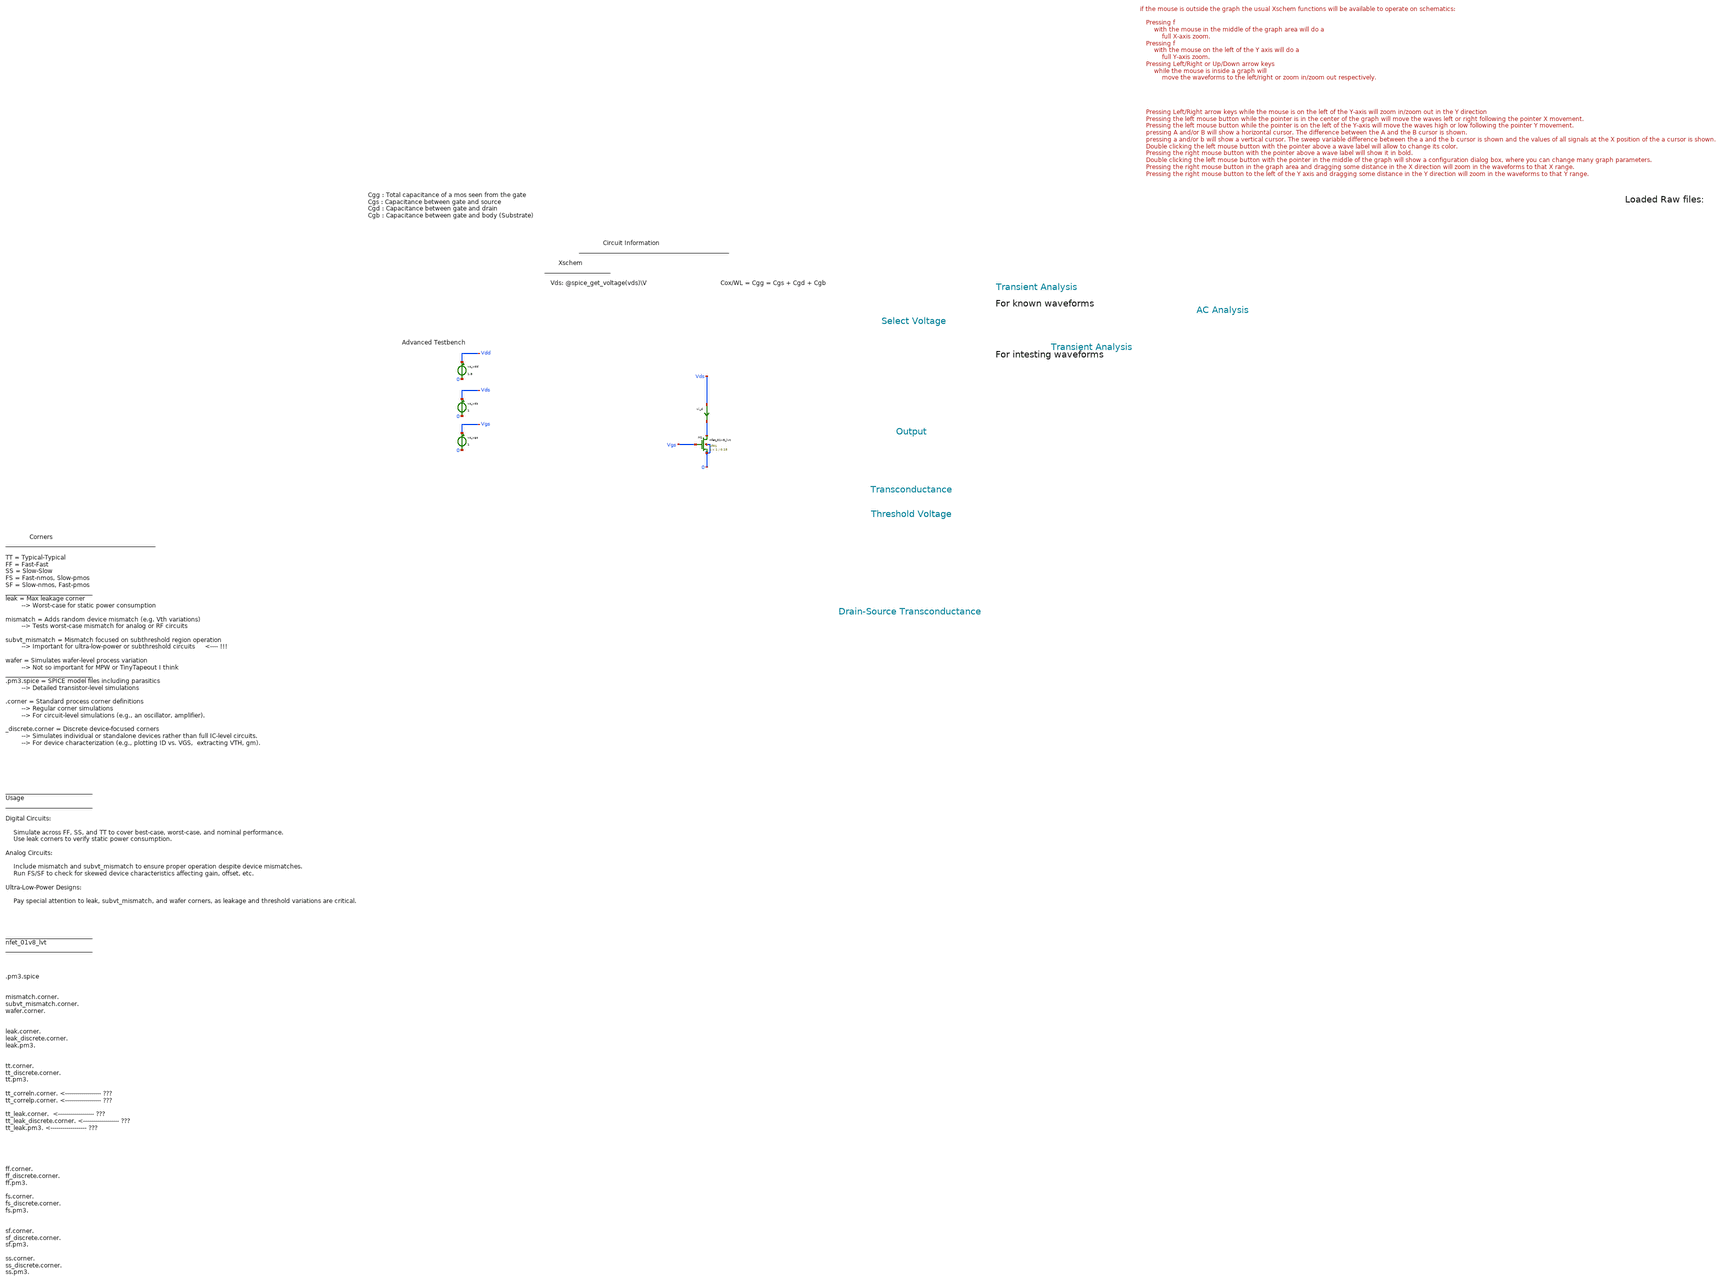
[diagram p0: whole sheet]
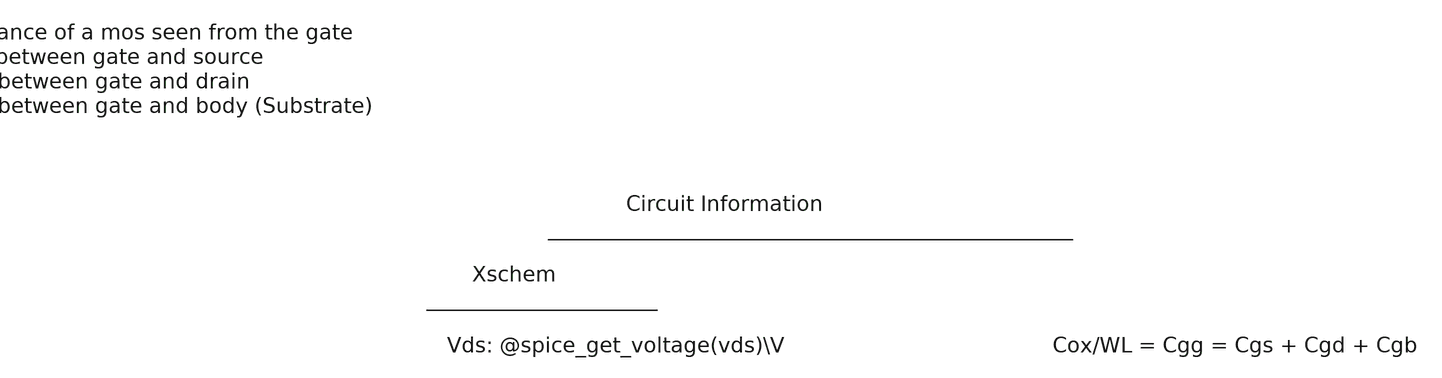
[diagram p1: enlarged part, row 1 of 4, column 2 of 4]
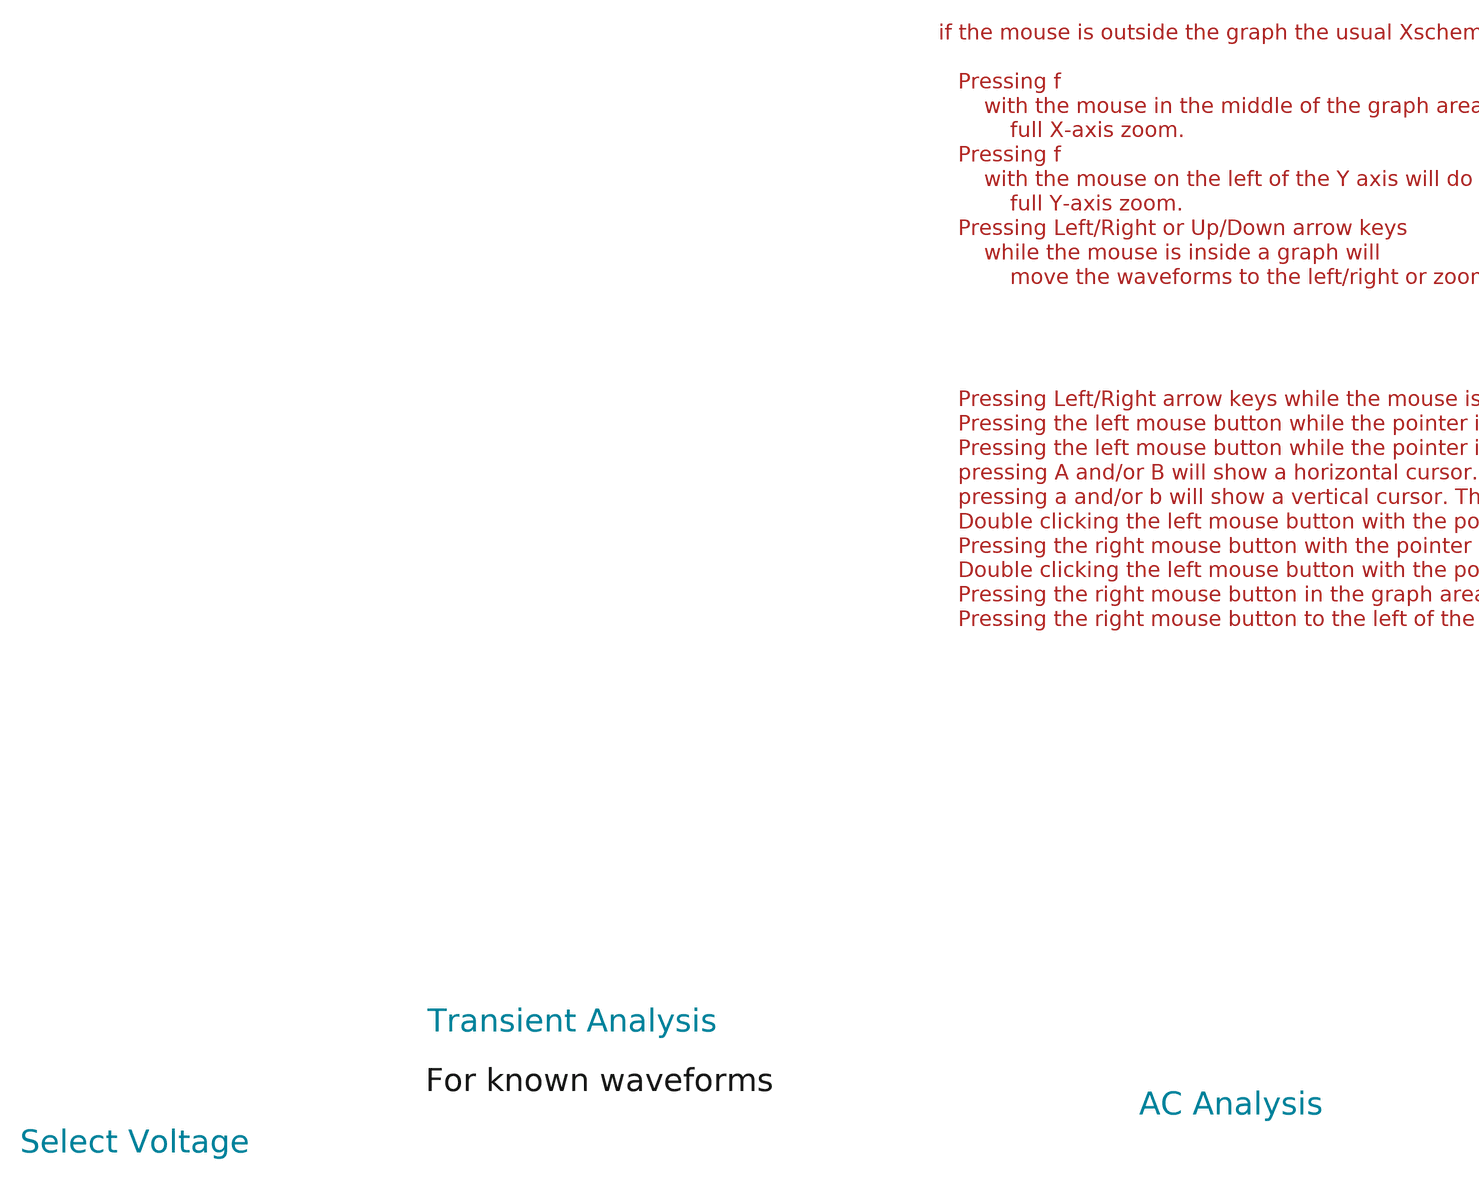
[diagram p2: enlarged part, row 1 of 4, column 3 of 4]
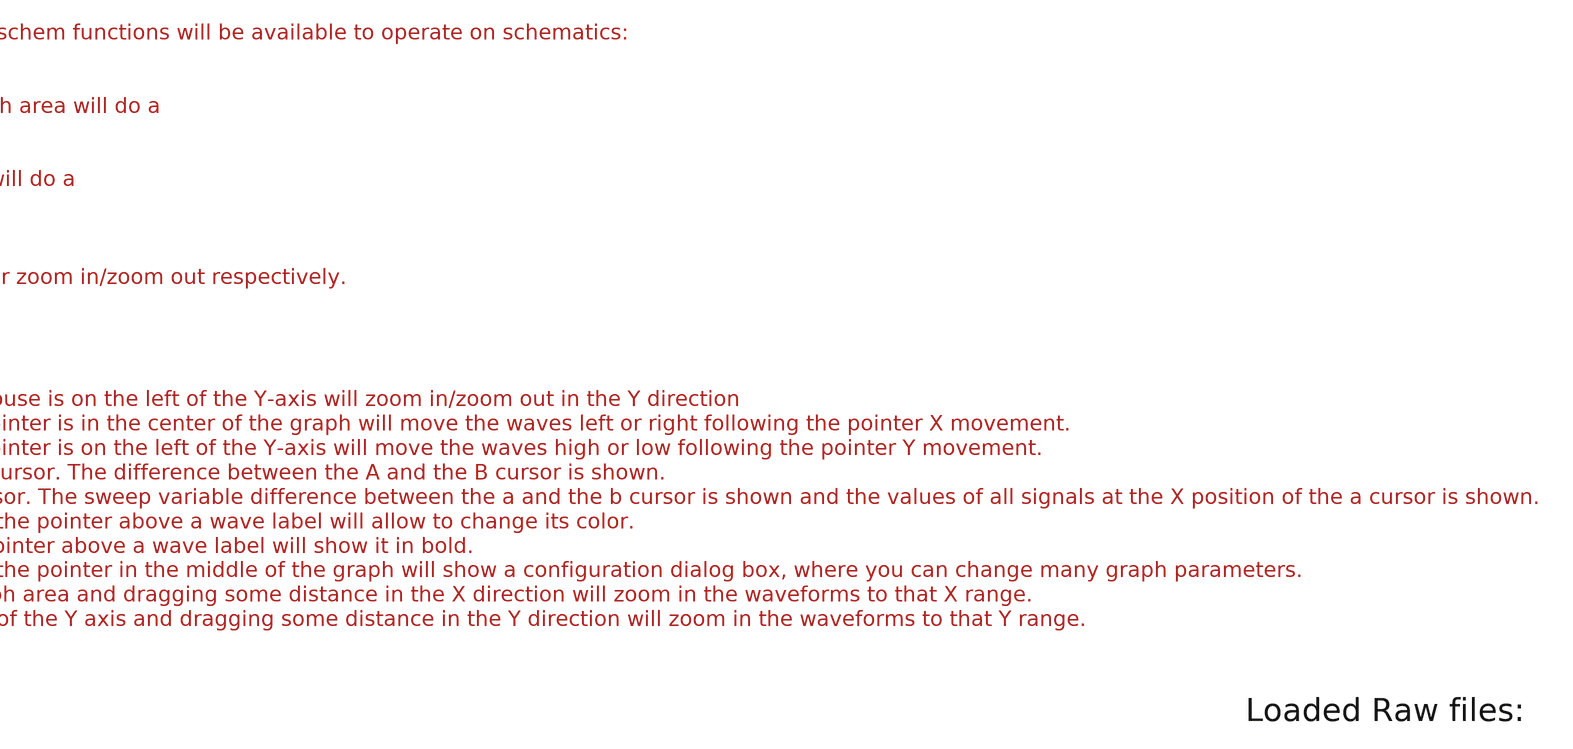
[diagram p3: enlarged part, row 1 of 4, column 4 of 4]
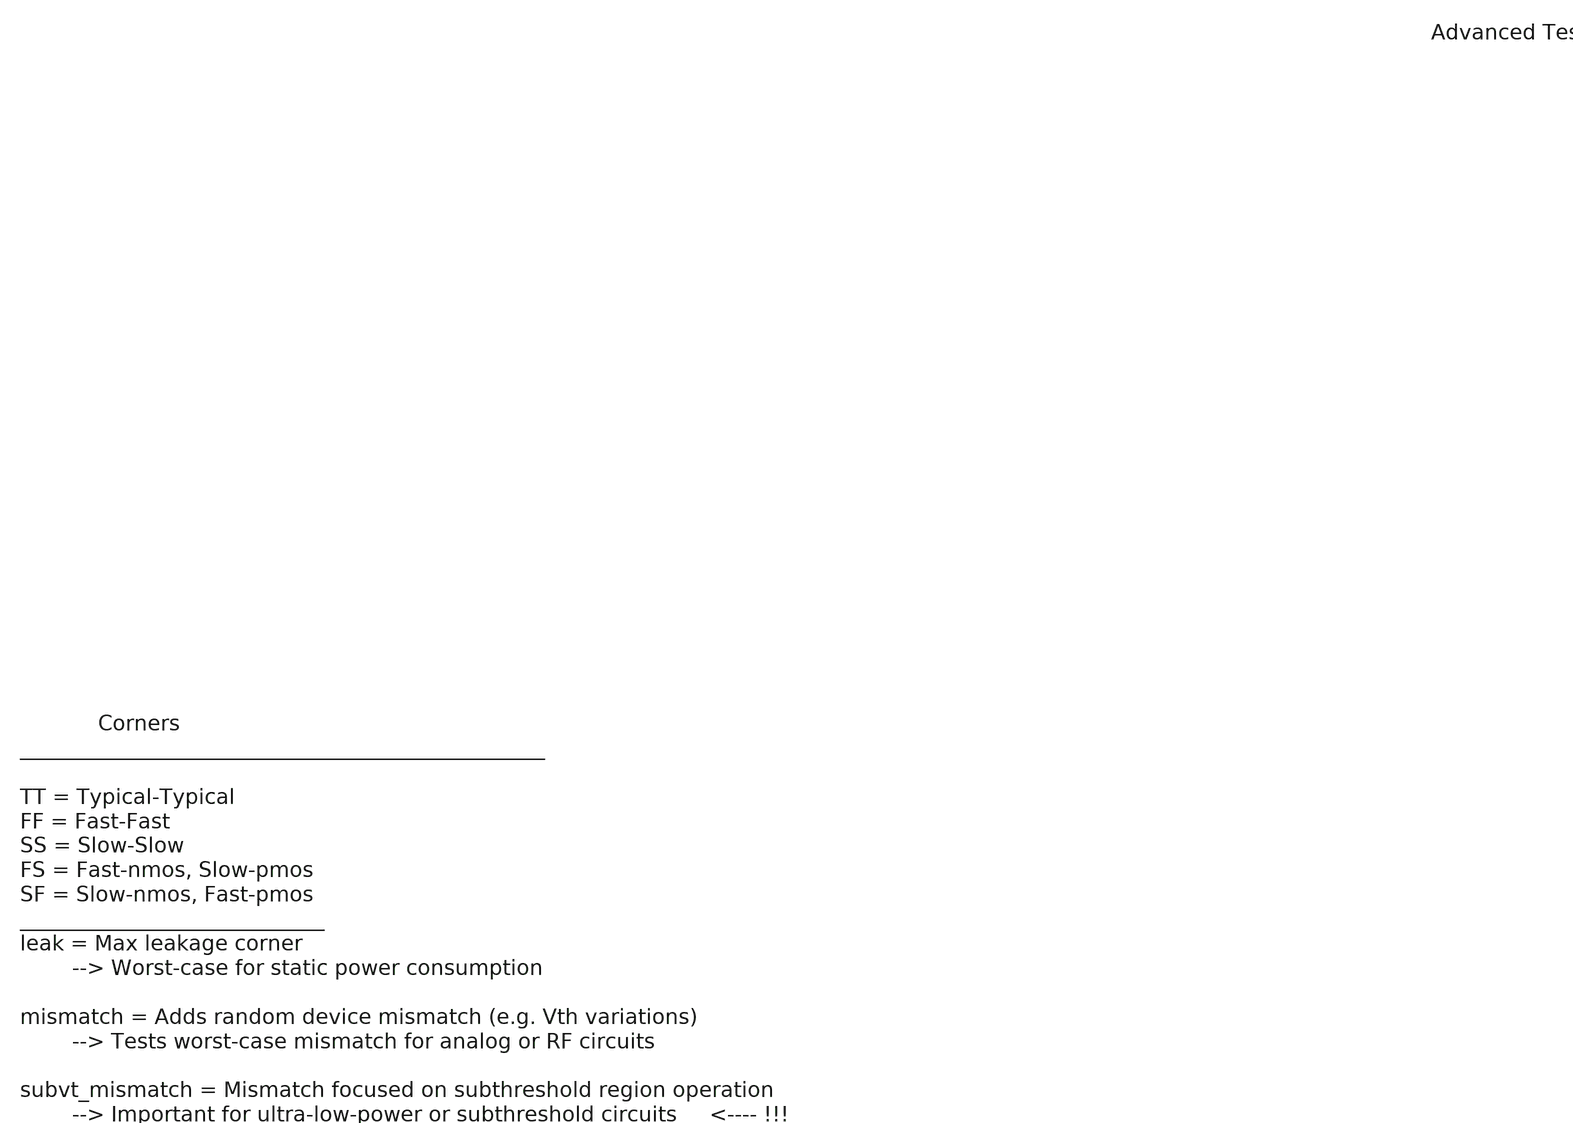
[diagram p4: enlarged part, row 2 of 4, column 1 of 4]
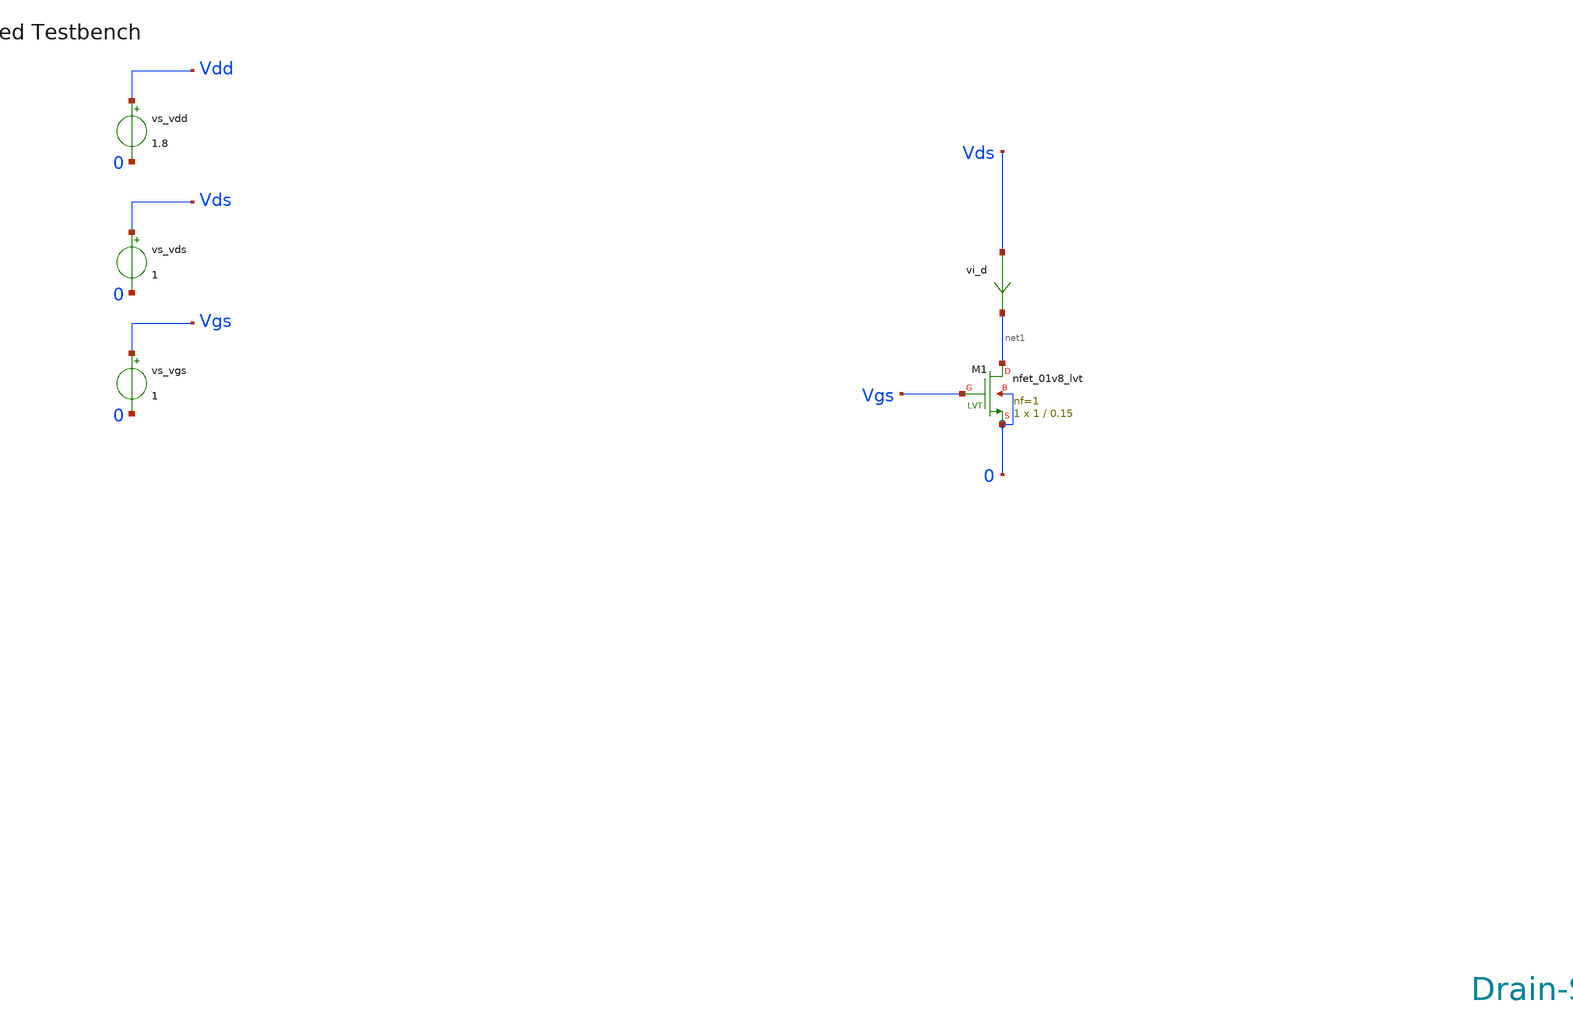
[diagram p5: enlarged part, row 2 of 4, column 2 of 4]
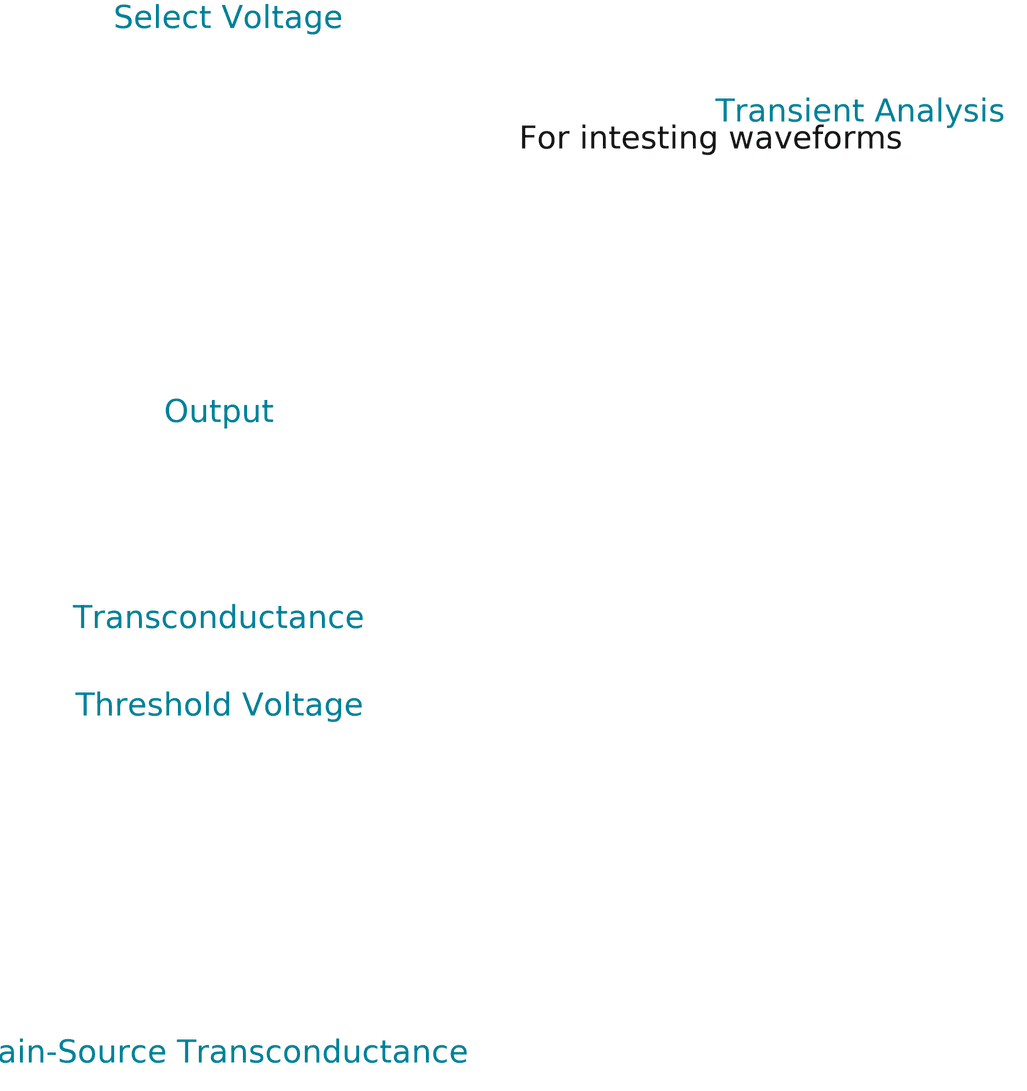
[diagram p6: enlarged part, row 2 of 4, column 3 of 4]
** sch_path: tt10-hdl/tt_um_test_commit/xschem/T0/nmos_lvt.sch
* Copyright (C) 1998-2024 Stefan Frederik Schippers
* This program is free software; you can redistribute it and/or modify
* it under the terms of the GNU General Public License as published by
* the Free Software Foundation; either version 2 of the License, or
* (at your option) any later version.
* This program is distributed in the hope that it will be useful,
* but WITHOUT ANY WARRANTY; without even the implied warranty of
* MERCHANTABILITY or FITNESS FOR A PARTICULAR PURPOSE.  See the
* GNU General Public License for more details.
* You should have received a copy of the GNU General Public License
* along with this program; if not, write to the Free Software
**.subckt nmos_lvt
vs_vgs Vgs 0 1
vs_vds Vds 0 1
vs_vdd Vdd 0 1.8
vi_d Vds net1 0
.save i(vi_d)
XM1 net1 Vgs 0 0 sky130_fd_pr__nfet_01v8_lvt L=0.15 W=1 nf=1 ad='int((1 + 1)/2) * 1 / 1 * 0.29' as='int((1 + 2)/2) * 1 / 1 * 0.29'
+ pd='2*int((1 + 1)/2) * (1 / 1 + 0.29)' ps='2*int((1 + 2)/2) * (1 / 1 + 0.29)' nrd='0.29 / 1 ' nrs='0.29 / 1 '
+ sa=0 sb=0 sd=0 mult=1 m=1
**** begin user architecture code



.temp 30

.param nw = 2
.param nl = 0.3
.param pw = 1
.param pl = 0.6

*.option gmin=5n
*.option scale=1e-6
*.option wnflag=1
.option savecurrents

.save all
.control
  save all alli

  save @m.xm1.msky130_fd_pr__nfet_01v8_lvt[gm]
  save @m.xm1.msky130_fd_pr__nfet_01v8_lvt[id]
  save @m.xm1.msky130_fd_pr__nfet_01v8_lvt[vgs]

  save @m.xm1.msky130_fd_pr__nfet_01v8_lvt[cgg]
  save @m.xm1.msky130_fd_pr__nfet_01v8_lvt[cgs]
  save @m.xm1.msky130_fd_pr__nfet_01v8_lvt[cgd]
  save @m.xm1.msky130_fd_pr__nfet_01v8_lvt[cgb]

  save @m.xm1.msky130_fd_pr__nfet_01v8_lvt[vds]
  save @m.xm1.msky130_fd_pr__nfet_01v8_lvt[vdsat]
  save @m.xm1.msky130_fd_pr__nfet_01v8_lvt[vth]


  save @m.xm1.msky130_fd_pr__nfet_01v8_lvt[leff]
  save @m.xm1.msky130_fd_pr__nfet_01v8_lvt[weff]
  save @m.xm1.msky130_fd_pr__nfet_01v8_lvt[gds]
  save @m.xm1.msky130_fd_pr__nfet_01v8_lvt[l]
  save @m.xm1.msky130_fd_pr__nfet_01v8_lvt[w]
  save @m.xm1.msky130_fd_pr__nfet_01v8_lvt[gm]
  save @m.xm1.msky130_fd_pr__nfet_01v8_lvt[gm]
  save @m.xm1.msky130_fd_pr__nfet_01v8_lvt[gm]
  save @m.xm1.msky130_fd_pr__nfet_01v8_lvt[gm]
  save @m.xm1.msky130_fd_pr__nfet_01v8_lvt[gm]


  dc vs_vds 0 0.6  0.005 vs_vgs 0 0.6 0.05
  *dc v_dev_vds 0 20u  10n
  write nmos_tb.raw


  op
  set appendwrite
  write nmos_tb.raw



  *tran 1n 5u
  *write nmos_tb.raw






  *quit 0




.endc





** opencircuitdesign pdks install
.lib $::SKYWATER_MODELS/sky130.lib.spice tt
.include $::SKYWATER_STDCELLS/sky130_fd_sc_hd.spice


**** end user architecture code
**.ends
.end
